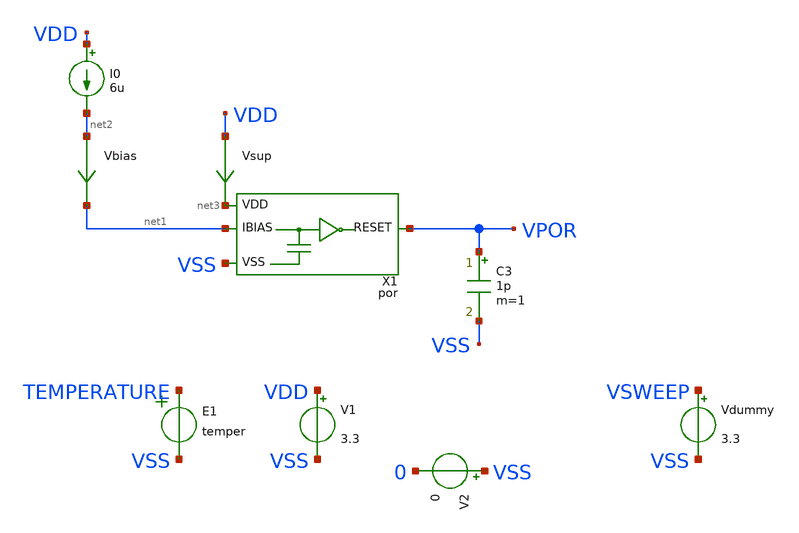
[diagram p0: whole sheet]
** sch_path: ip/por/xschem/por_tb.sch
**.subckt por_tb
V1 VDD VSS 3.3
V2 VSS 0 0
E1 TEMPERATURE VSS VOL=' temper '
X1 net3 VSS VPOR net1 por
C3 VPOR VSS 1p m=1
I0 VDD net2 6u
Vbias net2 net1 0
.save i(vbias)
Vsup VDD net3 0
.save i(vsup)
Vdummy VSWEEP VSS 3.3
**** begin user architecture code


.csparam TB_ID=${::TB_ID}
.csparam MC_RUNS=${::MC_RUNS}
.csparam EXIT_NGSPICE=${::EXIT_NGSPICE}
.lib ${::IHP_MODELS}/sg13g2.lib ${::CORNER}



* this experimental option enables mos model bin
* selection based on W/NF instead of W
.option wnflag=0

.control
* option savecurrents
*save all

define aunif(nom, avar) (nom + avar * sunif(0))

* dummy block for goto
if (1)
if TB_ID = 0
	goto TRAN_STARTUP
end
if TB_ID = 1
	goto TRAN_STARTUP
end

****************************************
label TRAN_STARTUP
****************************************
if MC_RUNS = 0
	let veclen=3
	let startup_t = vector(veclen)
	let run=0
	foreach v_sweep 1.8 2.5 3.3
	*foreach v_sweep 3.3
		save VPOR, VSWEEP
		alter vdummy=$v_sweep
		alter @v1[pwl] = [ 0 0 0.1u 0 1u $v_sweep]
		alter @I0[pwl] = [ 0 0 0.1u 0 0.5u 6u]
  		tran 100n 15m
		*plot v.x1.vmeas1#branch
		*plot vbias#branch
		*plot vsup#branch
  		plot VPOR
		*plot VDD
		*plot x1.vp
		meas tran m_up when VPOR=1 fall=1
		let startup_t[run] = m_up
		write tran.raw all
		let run = run + 1
		set appendwrite
		reset
	end
	print startup_t > tran.csv
else
	let startup_t = vector(MC_RUNS)
	let run=0
	dowhile run < MC_RUNS
		echo MC-RUN: $&run
		let v_sweep = aunif(2.55, 0.75)
		alter vdummy = $&v_sweep
		alter @v1[pwl] = [ 0 0 0.1u 0 1u $&v_sweep ]
		alter @I0[pwl] = [ 0 0 0.1u 0 0.5u 6u]
		save VPOR
		tran 100n 15m
		*plot VPOR
		meas tran m_up when VPOR=1 fall=1
		let startup_t[run] = m_up
 		reset
		let run = run + 1
	end
	print startup_t > tran.csv
end
goto done

****************************************
label done
****************************************
if EXIT_NGSPICE > 0.0
	exit
end
end
.endc


**** end user architecture code
**.ends

* expanding   symbol:  por.sym # of pins=4
** sym_path: ip/por/xschem/por.sym
** sch_path: ip/por/xschem/por.sch
.subckt por VDD VSS RESET IBIAS
*.iopin VSS
*.iopin VDD
*.opin RESET
*.ipin IBIAS
XM8 net1 net1 VDD VDD sg13_hv_pmos w=10u l=0.8u ng=1 m=1 mm_ok=1
Vmeas1 vp net10 0
.save i(vmeas1)
XM12 net2 net2 net1 VDD sg13_hv_pmos w=1u l=0.8u ng=1 m=1 mm_ok=1
XM1 IBIAS IBIAS VSS VSS sg13_hv_nmos w=10u l=0.8u ng=1 m=1 mm_ok=1
XM2 net2 IBIAS VSS VSS sg13_hv_nmos w=1u l=0.8u ng=1 m=1 mm_ok=1
XM9 net3 net1 VDD VDD sg13_hv_pmos w=1u l=0.8u ng=1 m=1 mm_ok=1
XM13 net4 net2 net3 VDD sg13_hv_pmos w=1u l=0.8u ng=1 m=1 mm_ok=1
XM3 net4 net4 VSS VSS sg13_hv_nmos w=10u l=0.8u ng=1 m=1 mm_ok=1
XM10 net5 net5 VDD VDD sg13_hv_pmos w=10u l=0.8u ng=1 m=1 mm_ok=1
XM14 net6 net6 net5 VDD sg13_hv_pmos w=1u l=0.8u ng=1 m=1 mm_ok=1
XM4 net6 net4 VSS VSS sg13_hv_nmos w=1u l=0.8u ng=1 m=1 mm_ok=1
XM11 net7 net5 VDD VDD sg13_hv_pmos w=1u l=0.8u ng=1 m=1 mm_ok=1
XM15 vp net6 net7 VDD sg13_hv_pmos w=1u l=0.8u ng=1 m=1 mm_ok=1
XC1 VSS net10 cap_cmim w=20e-6 l=20e-6 m=8 mm_ok=1
XM16 net8 vp VDD VDD sg13_hv_pmos w=10u l=0.8u ng=1 m=1 mm_ok=1
XM17 RESET vp net8 VDD sg13_hv_pmos w=10u l=0.8u ng=1 m=1 mm_ok=1
XM5 net9 vp VSS VSS sg13_hv_nmos w=10u l=0.8u ng=1 m=1 mm_ok=1
XM6 RESET vp net9 VSS sg13_hv_nmos w=10u l=0.8u ng=1 m=1 mm_ok=1
XM18 VSS RESET net8 VDD sg13_hv_pmos w=0.5u l=0.8u ng=1 m=1 mm_ok=1
XM7 VDD RESET net9 VSS sg13_hv_nmos w=0.5u l=0.8u ng=1 m=1 mm_ok=1
.ends

.end
